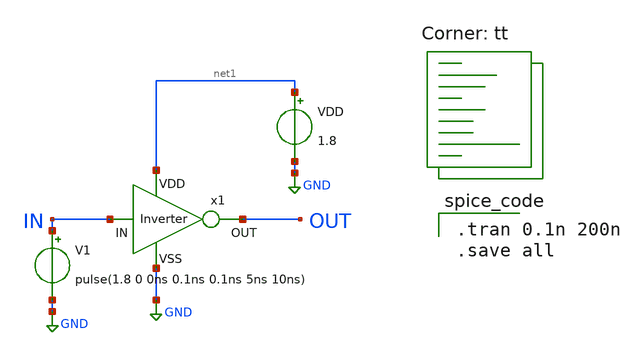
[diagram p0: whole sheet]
** sch_path: Inverter_tb.sch
**.subckt Inverter_tb
x1 net1 IN OUT GND Inverter
VDD net1 GND 1.8
V1 IN GND pulse(1.8 0 0ns 0.1ns 0.1ns 5ns 10ns)
**** begin user architecture code
.lib $::SKYWATER_MODELS/sky130.lib.spice tt

.tran 0.1n 200n
.save all


**** end user architecture code
**.ends

* expanding   symbol:  project/Inverter.sym # of pins=4
** sym_path: Inverter.sym
** sch_path: Inverter.sch
.subckt Inverter VDD IN OUT VSS
*.ipin IN
*.ipin VSS
*.ipin VDD
*.opin OUT
XM1 OUT IN VSS VSS sky130_fd_pr__nfet_01v8 L=0.3 W=1 nf=1 ad='int((nf+1)/2) * W/nf * 0.29' as='int((nf+2)/2) * W/nf * 0.29'
+ pd='2*int((nf+1)/2) * (W/nf + 0.29)' ps='2*int((nf+2)/2) * (W/nf + 0.29)' nrd='0.29 / W' nrs='0.29 / W'
+ sa=0 sb=0 sd=0 mult=1 m=1
XM2 OUT IN VDD VDD sky130_fd_pr__pfet_01v8 L=0.3 W=2 nf=1 ad='int((nf+1)/2) * W/nf * 0.29' as='int((nf+2)/2) * W/nf * 0.29'
+ pd='2*int((nf+1)/2) * (W/nf + 0.29)' ps='2*int((nf+2)/2) * (W/nf + 0.29)' nrd='0.29 / W' nrs='0.29 / W'
+ sa=0 sb=0 sd=0 mult=1 m=1
.ends

.GLOBAL GND
.end
